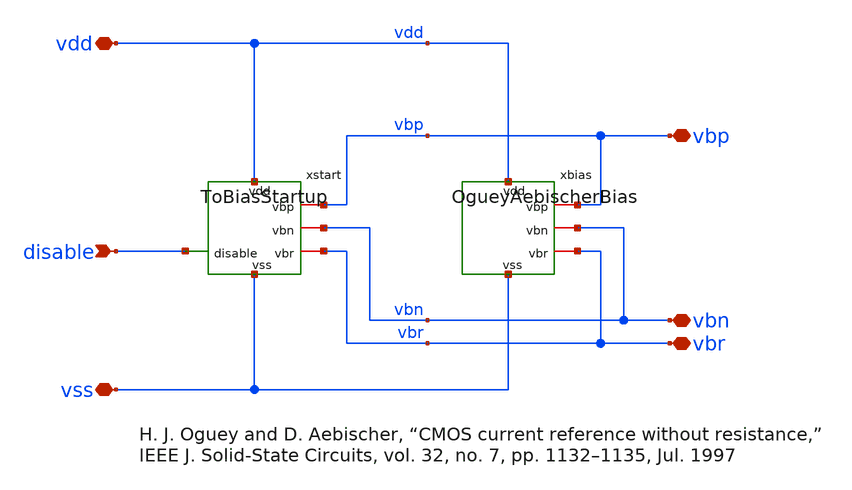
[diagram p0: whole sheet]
** sch_path: sudelbuecher/design_considerations/consolidation/reference_sheets_2026-10-20/macros/OgueyAebischerBias/schematic/xschem/reference.sch
**.subckt reference vss vdd vbp vbn vbr disable
*.iopin vss
*.iopin vdd
*.iopin vbp
*.iopin vbn
*.iopin vbr
*.ipin disable
xbias vdd vbp vbn vbr vss OgueyAebischerBias
xstart vdd vbp vbn disable vbr vss ToBiasStartup
**.ends
.end
